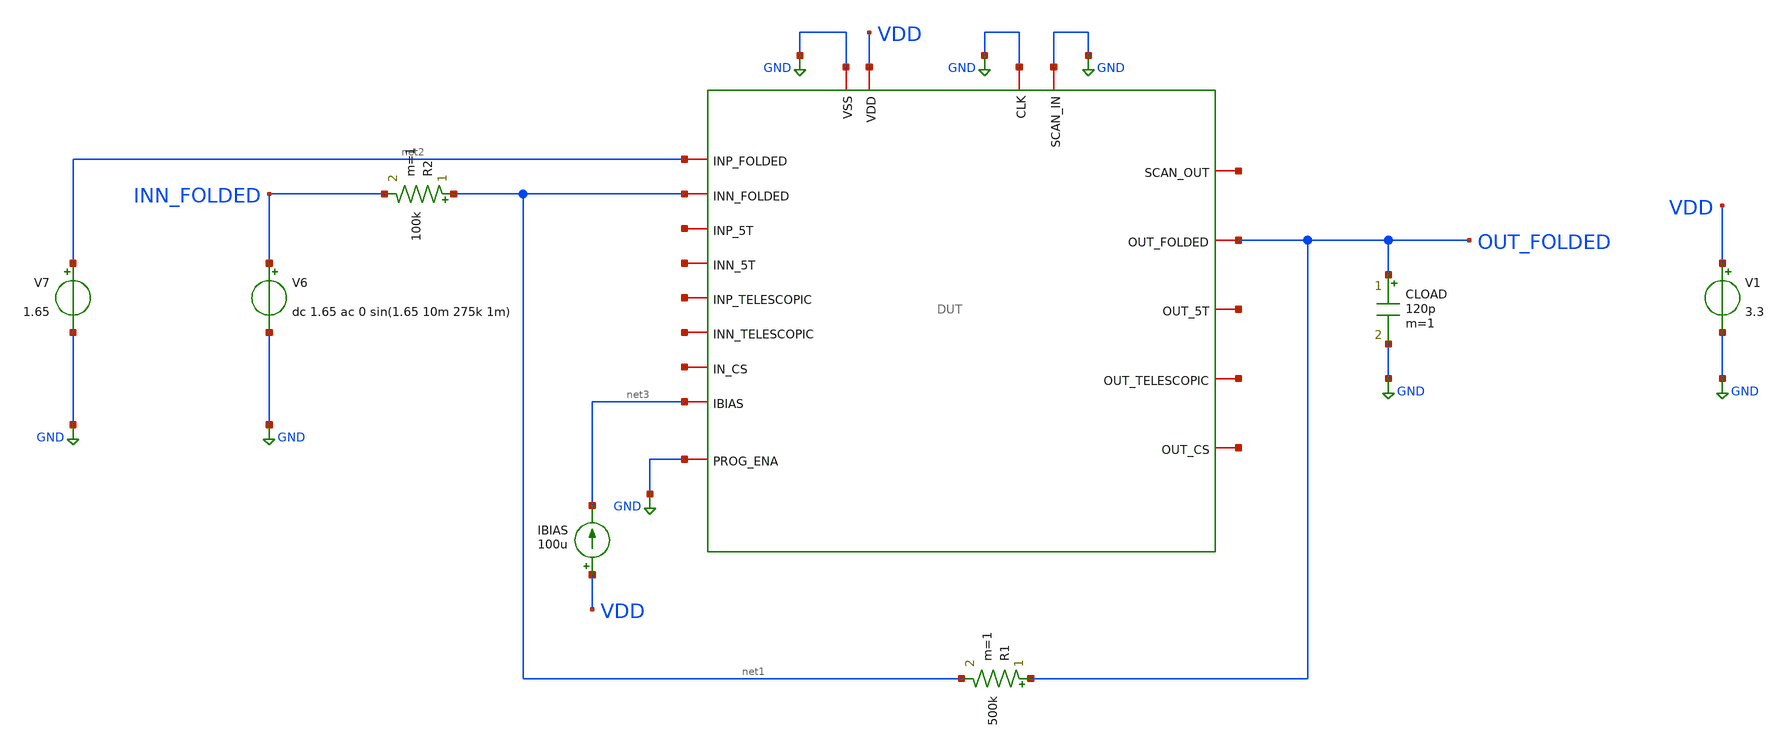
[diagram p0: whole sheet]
** sch_path: designs/libs/verification/ota_folded/default_sizing/bandwidth_tb.sch
**.subckt bandwidth_tb
x1 GND net4 GND GND VDD OUT_FOLDED net2 net5 net3 net1 net6 net7 net8 net9 net10 net11 net12 GND DUT
V1 VDD GND 3.3
CLOAD OUT_FOLDED GND 120p m=1
R1 OUT_FOLDED net1 500k m=1
R2 net1 INN_FOLDED 100k m=1
V6 INN_FOLDED GND dc 1.65 ac 0 sin(1.65 10m 275k 1m)
V7 net2 GND 1.65
IBIAS VDD net3 100u
**** begin user architecture code

.include $::180MCU_MODELS/design.ngspice
.lib $::180MCU_MODELS/sm141064.ngspice typical



.control
tran 1u 5m

meas tran vout_pp pp v(out_folded) from=2m to=5m
meas tran vin_pp pp v(inn_folded) from=2m to=5m
let gain = vout_pp / vin_pp
let gain_db = 20 * log(gain) / log(10)
print gain gain_db
.endc


**** end user architecture code
**.ends
.GLOBAL GND
.end
